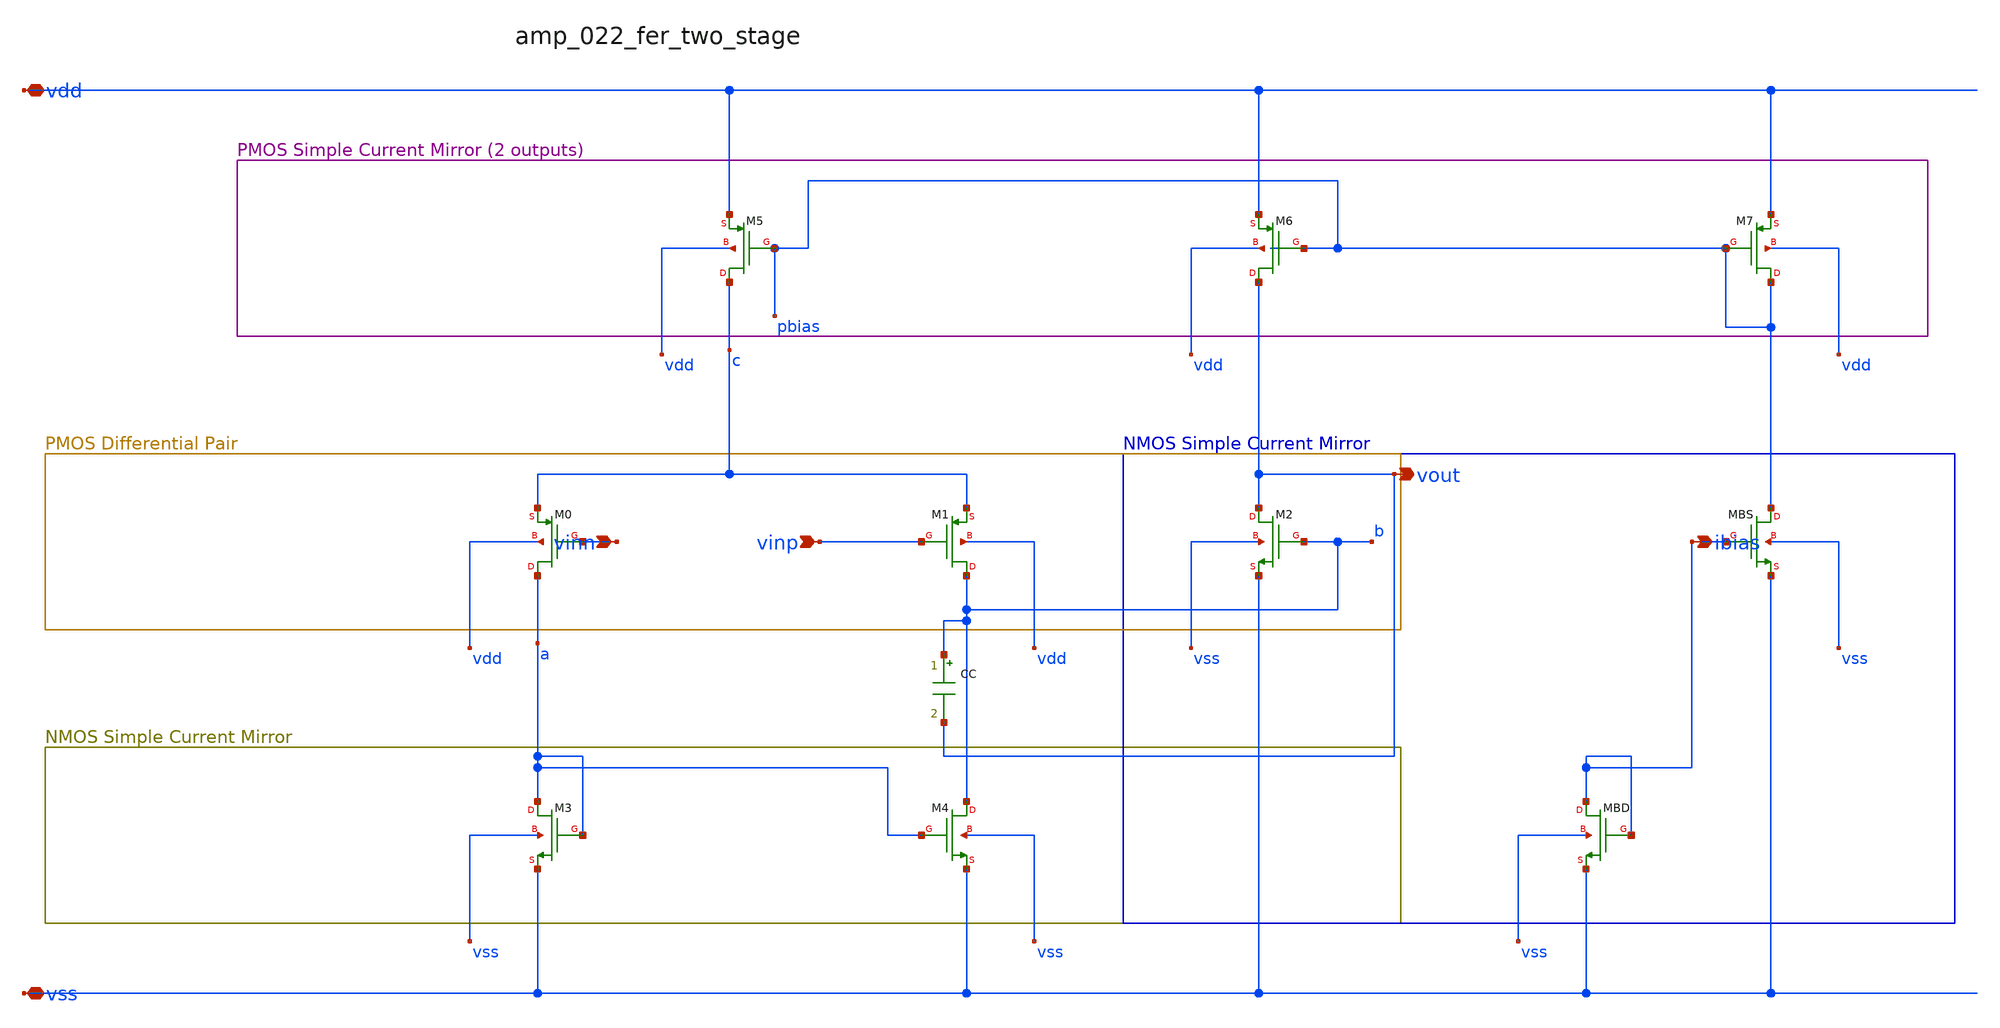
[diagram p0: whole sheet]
** sch_path: analog-db/raw/amp_022_fer_two_stage/amp_022_fer_two_stage_annotated.sch
**.subckt amp_022_fer_two_stage_annotated vinn vinp vdd vss vout ibias
*.ipin vinn
*.ipin vinp
*.iopin vdd
*.iopin vss
*.opin vout
*.opin ibias
CC b vout x_dut_cc_value m=1
XM0 a vinn c vdd sg13_lv_pmos w=x_dut_xm0_w l=x_dut_xm0_l ng=1 m=x_dut_xm0_m
XM1 b vinp c vdd sg13_lv_pmos w=x_dut_xm1_w l=x_dut_xm1_l ng=1 m=x_dut_xm1_m
XM2 vout b vss vss sg13_lv_nmos w=x_dut_xm2_w l=x_dut_xm2_l ng=1 m=x_dut_xm2_m
XM3 a a vss vss sg13_lv_nmos w=x_dut_xm3_w l=x_dut_xm3_l ng=1 m=x_dut_xm3_m
XM4 b a vss vss sg13_lv_nmos w=x_dut_xm4_w l=x_dut_xm4_l ng=1 m=x_dut_xm4_m
XM5 c pbias vdd vdd sg13_lv_pmos w=x_dut_xm5_w l=x_dut_xm5_l ng=1 m=x_dut_xm5_m
XM6 vout pbias vdd vdd sg13_lv_pmos w=x_dut_xm6_w l=x_dut_xm6_l ng=1 m=x_dut_xm6_m
XM7 pbias pbias vdd vdd sg13_lv_pmos w=x_dut_xm7_w l=x_dut_xm7_l ng=1 m=x_dut_xm7_m
XMBD ibias ibias vss vss sg13_lv_nmos w=x_dut_xmbd_w l=x_dut_xmbd_l ng=1 m=x_dut_xmbd_m
XMBS pbias ibias vss vss sg13_lv_nmos w=x_dut_xmbs_w l=x_dut_xmbs_l ng=1 m=x_dut_xmbs_m
**.ends
.end
